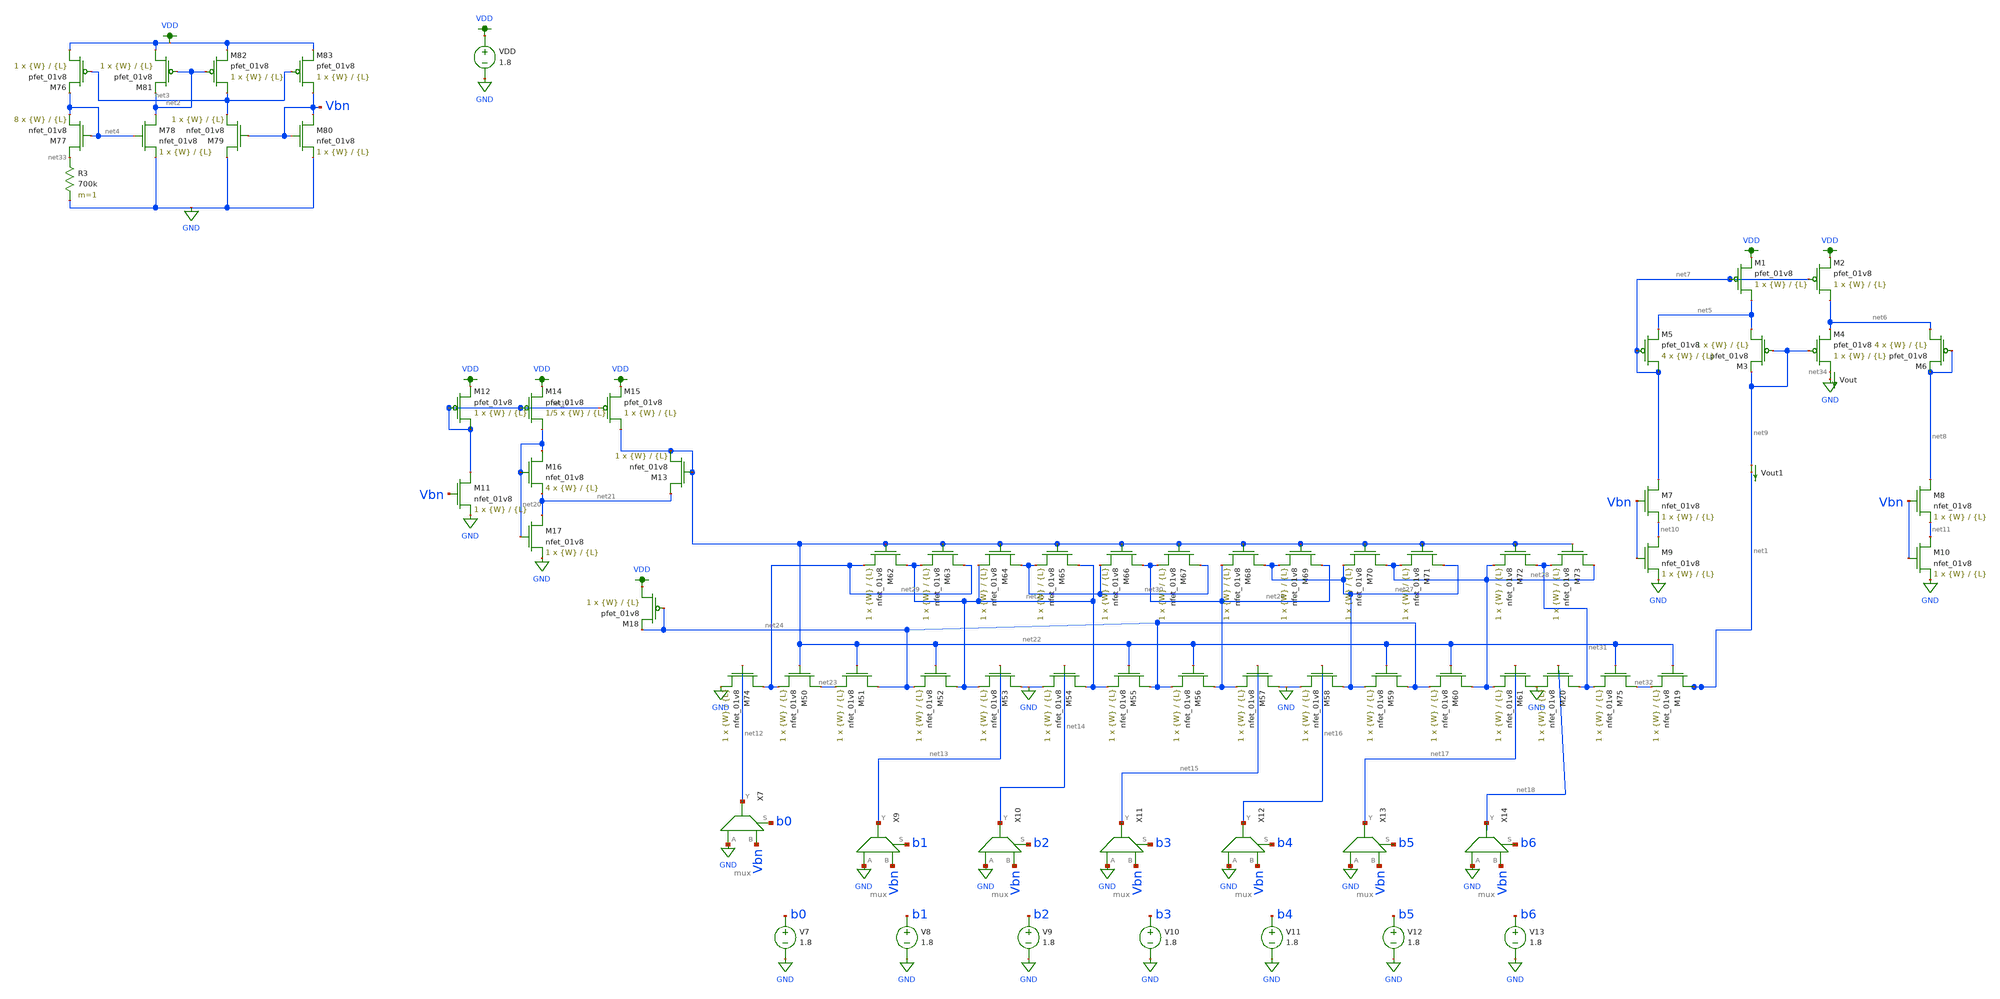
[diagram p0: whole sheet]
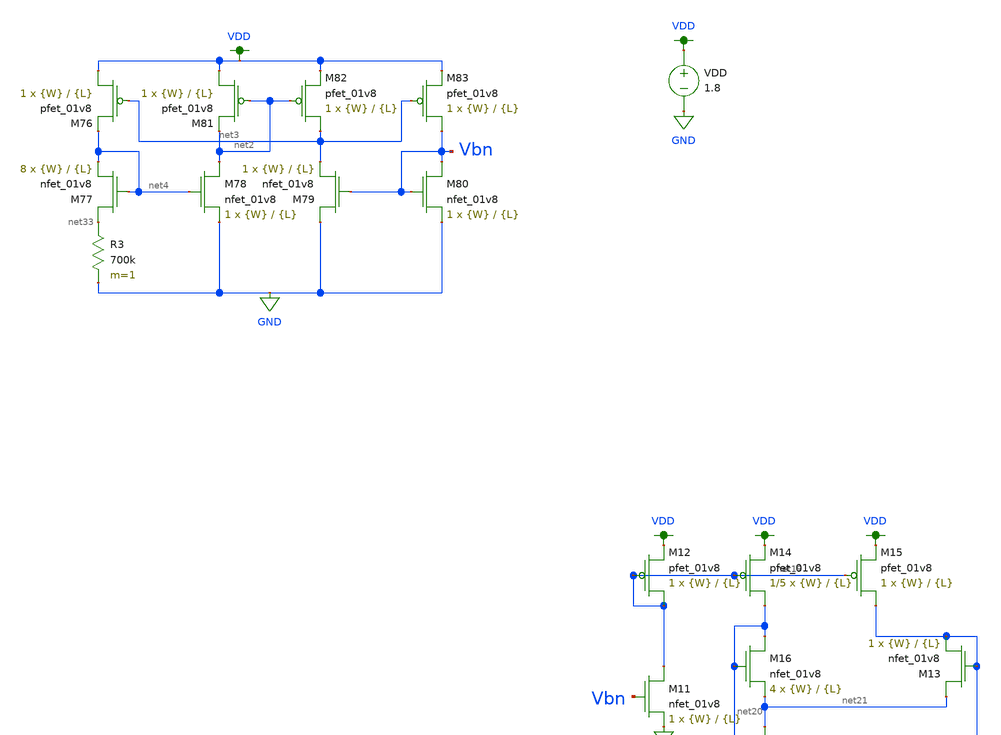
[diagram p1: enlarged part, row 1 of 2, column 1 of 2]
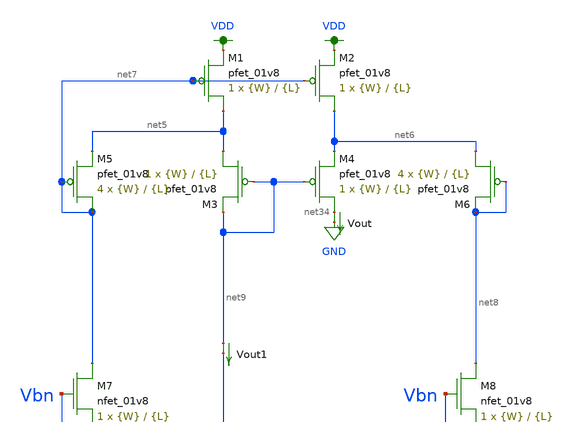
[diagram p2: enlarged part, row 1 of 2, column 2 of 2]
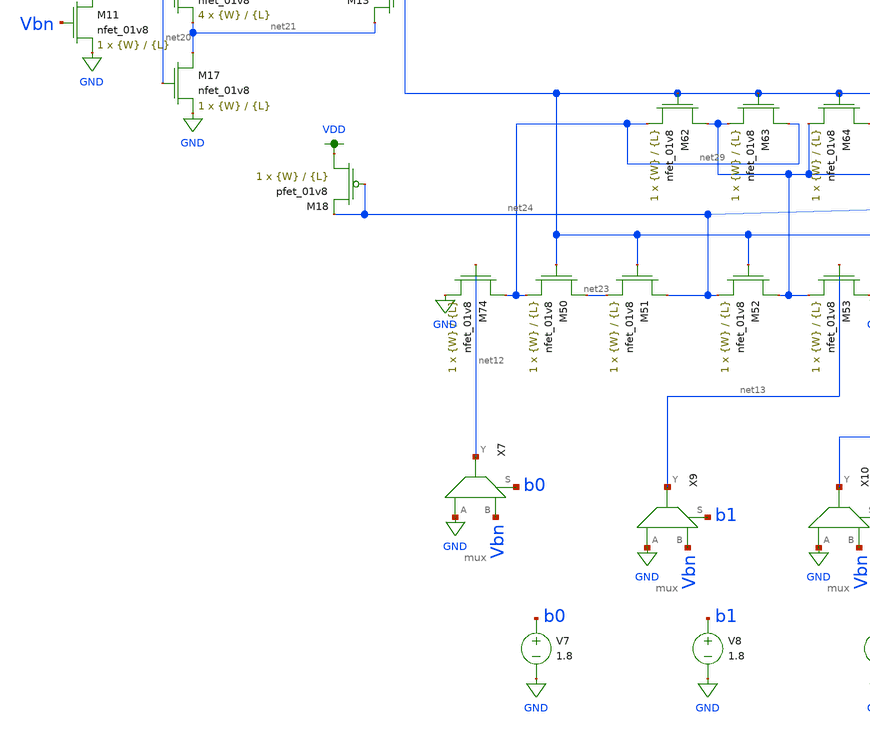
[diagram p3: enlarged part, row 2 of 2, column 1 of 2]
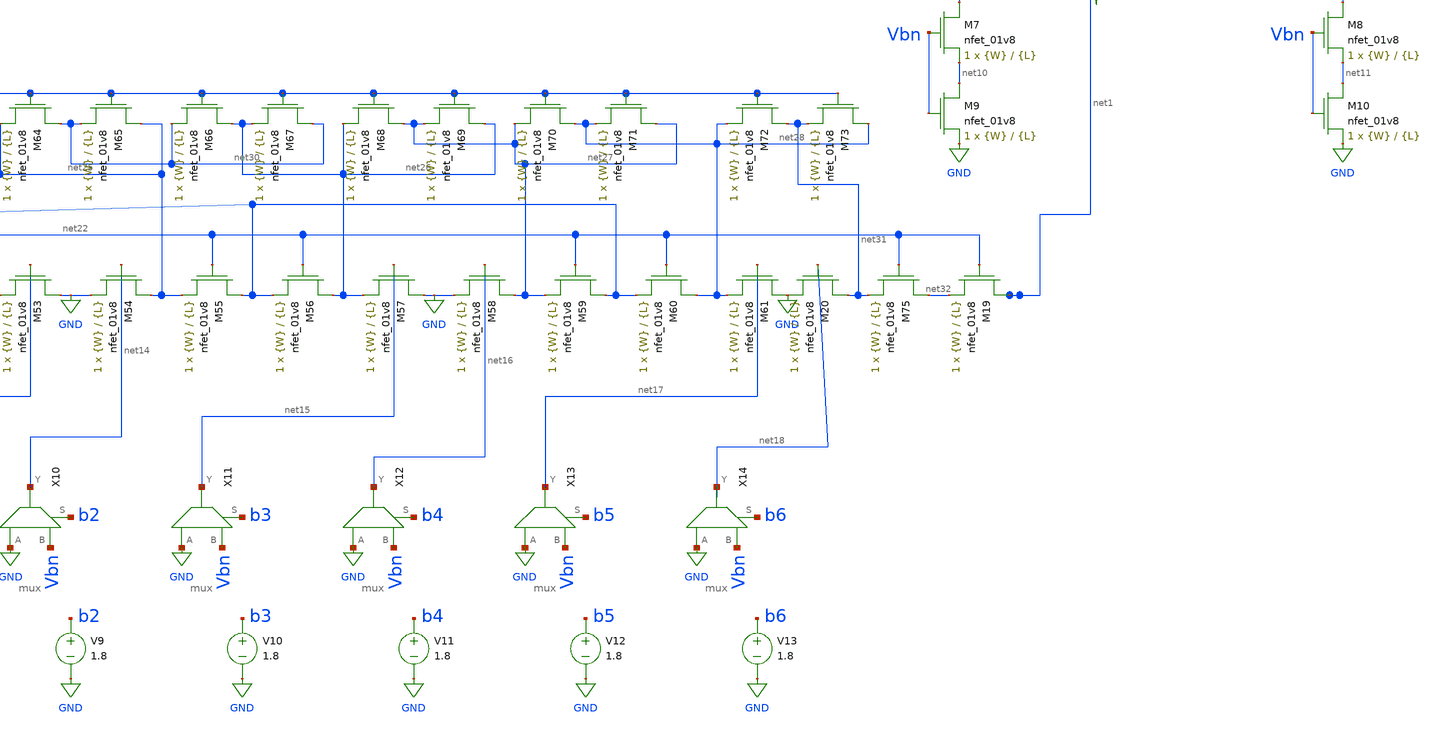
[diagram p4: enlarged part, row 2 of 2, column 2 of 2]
** sch_path: dac/schematics/misc/dac_lds_sim.sch
**.subckt dac_lds_sim
VDD VDD GND 1.8
XM76 VDD net3 net4 VDD sky130_fd_pr__pfet_01v8 L={L} W={W} nf=1 ad='int((nf+1)/2) * W/nf * 0.29' as='int((nf+2)/2) * W/nf * 0.29'
+ pd='2*int((nf+1)/2) * (W/nf + 0.29)' ps='2*int((nf+2)/2) * (W/nf + 0.29)' nrd='0.29 / W' nrs='0.29 / W'
+ sa=0 sb=0 sd=0 mult=1 m=1
XM77 net33 net4 net4 GND sky130_fd_pr__nfet_01v8 L={L} W={W} nf=1 ad='int((nf+1)/2) * W/nf * 0.29' as='int((nf+2)/2) * W/nf * 0.29'
+ pd='2*int((nf+1)/2) * (W/nf + 0.29)' ps='2*int((nf+2)/2) * (W/nf + 0.29)' nrd='0.29 / W' nrs='0.29 / W'
+ sa=0 sb=0 sd=0 mult=8 m=8
R3 net33 GND 700k m=1
XM78 net2 net4 GND GND sky130_fd_pr__nfet_01v8 L={L} W={W} nf=1 ad='int((nf+1)/2) * W/nf * 0.29' as='int((nf+2)/2) * W/nf * 0.29'
+ pd='2*int((nf+1)/2) * (W/nf + 0.29)' ps='2*int((nf+2)/2) * (W/nf + 0.29)' nrd='0.29 / W' nrs='0.29 / W'
+ sa=0 sb=0 sd=0 mult=1 m=1
XM79 GND Vbn net3 GND sky130_fd_pr__nfet_01v8 L={L} W={W} nf=1 ad='int((nf+1)/2) * W/nf * 0.29' as='int((nf+2)/2) * W/nf * 0.29'
+ pd='2*int((nf+1)/2) * (W/nf + 0.29)' ps='2*int((nf+2)/2) * (W/nf + 0.29)' nrd='0.29 / W' nrs='0.29 / W'
+ sa=0 sb=0 sd=0 mult=1 m=1
XM80 Vbn Vbn GND GND sky130_fd_pr__nfet_01v8 L={L} W={W} nf=1 ad='int((nf+1)/2) * W/nf * 0.29' as='int((nf+2)/2) * W/nf * 0.29'
+ pd='2*int((nf+1)/2) * (W/nf + 0.29)' ps='2*int((nf+2)/2) * (W/nf + 0.29)' nrd='0.29 / W' nrs='0.29 / W'
+ sa=0 sb=0 sd=0 mult=1 m=1
XM81 VDD net2 net2 VDD sky130_fd_pr__pfet_01v8 L={L} W={W} nf=1 ad='int((nf+1)/2) * W/nf * 0.29' as='int((nf+2)/2) * W/nf * 0.29'
+ pd='2*int((nf+1)/2) * (W/nf + 0.29)' ps='2*int((nf+2)/2) * (W/nf + 0.29)' nrd='0.29 / W' nrs='0.29 / W'
+ sa=0 sb=0 sd=0 mult=1 m=1
XM82 net3 net2 VDD VDD sky130_fd_pr__pfet_01v8 L={L} W={W} nf=1 ad='int((nf+1)/2) * W/nf * 0.29' as='int((nf+2)/2) * W/nf * 0.29'
+ pd='2*int((nf+1)/2) * (W/nf + 0.29)' ps='2*int((nf+2)/2) * (W/nf + 0.29)' nrd='0.29 / W' nrs='0.29 / W'
+ sa=0 sb=0 sd=0 mult=1 m=1
XM83 Vbn net3 VDD VDD sky130_fd_pr__pfet_01v8 L={L} W={W} nf=1 ad='int((nf+1)/2) * W/nf * 0.29' as='int((nf+2)/2) * W/nf * 0.29'
+ pd='2*int((nf+1)/2) * (W/nf + 0.29)' ps='2*int((nf+2)/2) * (W/nf + 0.29)' nrd='0.29 / W' nrs='0.29 / W'
+ sa=0 sb=0 sd=0 mult=1 m=1
Vout net34 GND 0
.save i(vout)
XM1 net5 net7 VDD VDD sky130_fd_pr__pfet_01v8 L={L} W={W} nf=1 ad='int((nf+1)/2) * W/nf * 0.29' as='int((nf+2)/2) * W/nf * 0.29'
+ pd='2*int((nf+1)/2) * (W/nf + 0.29)' ps='2*int((nf+2)/2) * (W/nf + 0.29)' nrd='0.29 / W' nrs='0.29 / W'
+ sa=0 sb=0 sd=0 mult=1 m=1
XM2 net6 net7 VDD VDD sky130_fd_pr__pfet_01v8 L={L} W={W} nf=1 ad='int((nf+1)/2) * W/nf * 0.29' as='int((nf+2)/2) * W/nf * 0.29'
+ pd='2*int((nf+1)/2) * (W/nf + 0.29)' ps='2*int((nf+2)/2) * (W/nf + 0.29)' nrd='0.29 / W' nrs='0.29 / W'
+ sa=0 sb=0 sd=0 mult=1 m=1
XM3 net5 net9 net9 VDD sky130_fd_pr__pfet_01v8 L={L} W={W} nf=1 ad='int((nf+1)/2) * W/nf * 0.29' as='int((nf+2)/2) * W/nf * 0.29'
+ pd='2*int((nf+1)/2) * (W/nf + 0.29)' ps='2*int((nf+2)/2) * (W/nf + 0.29)' nrd='0.29 / W' nrs='0.29 / W'
+ sa=0 sb=0 sd=0 mult=1 m=1
XM4 net34 net9 net6 VDD sky130_fd_pr__pfet_01v8 L={L} W={W} nf=1 ad='int((nf+1)/2) * W/nf * 0.29' as='int((nf+2)/2) * W/nf * 0.29'
+ pd='2*int((nf+1)/2) * (W/nf + 0.29)' ps='2*int((nf+2)/2) * (W/nf + 0.29)' nrd='0.29 / W' nrs='0.29 / W'
+ sa=0 sb=0 sd=0 mult=1 m=1
XM5 net7 net7 net5 VDD sky130_fd_pr__pfet_01v8 L={L} W={W} nf=1 ad='int((nf+1)/2) * W/nf * 0.29' as='int((nf+2)/2) * W/nf * 0.29'
+ pd='2*int((nf+1)/2) * (W/nf + 0.29)' ps='2*int((nf+2)/2) * (W/nf + 0.29)' nrd='0.29 / W' nrs='0.29 / W'
+ sa=0 sb=0 sd=0 mult=4 m=4
XM6 net6 net8 net8 VDD sky130_fd_pr__pfet_01v8 L={L} W={W} nf=1 ad='int((nf+1)/2) * W/nf * 0.29' as='int((nf+2)/2) * W/nf * 0.29'
+ pd='2*int((nf+1)/2) * (W/nf + 0.29)' ps='2*int((nf+2)/2) * (W/nf + 0.29)' nrd='0.29 / W' nrs='0.29 / W'
+ sa=0 sb=0 sd=0 mult=4 m=4
XM7 net7 Vbn net10 GND sky130_fd_pr__nfet_01v8 L={L} W={W} nf=1 ad='int((nf+1)/2) * W/nf * 0.29' as='int((nf+2)/2) * W/nf * 0.29'
+ pd='2*int((nf+1)/2) * (W/nf + 0.29)' ps='2*int((nf+2)/2) * (W/nf + 0.29)' nrd='0.29 / W' nrs='0.29 / W'
+ sa=0 sb=0 sd=0 mult=1 m=1
XM8 net8 Vbn net11 GND sky130_fd_pr__nfet_01v8 L={L} W={W} nf=1 ad='int((nf+1)/2) * W/nf * 0.29' as='int((nf+2)/2) * W/nf * 0.29'
+ pd='2*int((nf+1)/2) * (W/nf + 0.29)' ps='2*int((nf+2)/2) * (W/nf + 0.29)' nrd='0.29 / W' nrs='0.29 / W'
+ sa=0 sb=0 sd=0 mult=1 m=1
XM9 net10 Vbn GND GND sky130_fd_pr__nfet_01v8 L={L} W={W} nf=1 ad='int((nf+1)/2) * W/nf * 0.29' as='int((nf+2)/2) * W/nf * 0.29'
+ pd='2*int((nf+1)/2) * (W/nf + 0.29)' ps='2*int((nf+2)/2) * (W/nf + 0.29)' nrd='0.29 / W' nrs='0.29 / W'
+ sa=0 sb=0 sd=0 mult=1 m=1
XM10 net11 Vbn GND GND sky130_fd_pr__nfet_01v8 L={L} W={W} nf=1 ad='int((nf+1)/2) * W/nf * 0.29' as='int((nf+2)/2) * W/nf * 0.29'
+ pd='2*int((nf+1)/2) * (W/nf + 0.29)' ps='2*int((nf+2)/2) * (W/nf + 0.29)' nrd='0.29 / W' nrs='0.29 / W'
+ sa=0 sb=0 sd=0 mult=1 m=1
V7 b0 GND 1.8
V8 b1 GND 1.8
V9 b2 GND 1.8
V10 b3 GND 1.8
V11 b4 GND 1.8
V12 b5 GND 1.8
V13 b6 GND 1.8
X7 GND Vbn net12 b0 mux
X9 GND Vbn net13 b1 mux
X10 GND Vbn net14 b2 mux
X11 GND Vbn net15 b3 mux
X12 GND Vbn net16 b4 mux
X13 GND Vbn net17 b5 mux
X14 GND Vbn net18 b6 mux
XM11 net19 Vbn GND GND sky130_fd_pr__nfet_01v8 L={L} W={W} nf=1 ad='int((nf+1)/2) * W/nf * 0.29' as='int((nf+2)/2) * W/nf * 0.29'
+ pd='2*int((nf+1)/2) * (W/nf + 0.29)' ps='2*int((nf+2)/2) * (W/nf + 0.29)' nrd='0.29 / W' nrs='0.29 / W'
+ sa=0 sb=0 sd=0 mult=1 m=1
XM12 net19 net19 VDD VDD sky130_fd_pr__pfet_01v8 L={L} W={W} nf=1 ad='int((nf+1)/2) * W/nf * 0.29' as='int((nf+2)/2) * W/nf * 0.29'
+ pd='2*int((nf+1)/2) * (W/nf + 0.29)' ps='2*int((nf+2)/2) * (W/nf + 0.29)' nrd='0.29 / W' nrs='0.29 / W'
+ sa=0 sb=0 sd=0 mult=1 m=1
XM13 net21 net22 net22 GND sky130_fd_pr__nfet_01v8 L={L} W={W} nf=1 ad='int((nf+1)/2) * W/nf * 0.29'
+ as='int((nf+2)/2) * W/nf * 0.29' pd='2*int((nf+1)/2) * (W/nf + 0.29)' ps='2*int((nf+2)/2) * (W/nf + 0.29)'
+ nrd='0.29 / W' nrs='0.29 / W' sa=0 sb=0 sd=0 mult=1 m=1
XM14 net20 net19 VDD VDD sky130_fd_pr__pfet_01v8 L={L} W={W} nf=1 ad='int((nf+1)/2) * W/nf * 0.29' as='int((nf+2)/2) * W/nf * 0.29'
+ pd='2*int((nf+1)/2) * (W/nf + 0.29)' ps='2*int((nf+2)/2) * (W/nf + 0.29)' nrd='0.29 / W' nrs='0.29 / W'
+ sa=0 sb=0 sd=0 mult=1/5 m=1/5
XM15 net22 net19 VDD VDD sky130_fd_pr__pfet_01v8 L={L} W={W} nf=1 ad='int((nf+1)/2) * W/nf * 0.29' as='int((nf+2)/2) * W/nf * 0.29'
+ pd='2*int((nf+1)/2) * (W/nf + 0.29)' ps='2*int((nf+2)/2) * (W/nf + 0.29)' nrd='0.29 / W' nrs='0.29 / W'
+ sa=0 sb=0 sd=0 mult=1 m=1
XM16 net20 net20 net21 GND sky130_fd_pr__nfet_01v8 L={L} W={W} nf=1 ad='int((nf+1)/2) * W/nf * 0.29'
+ as='int((nf+2)/2) * W/nf * 0.29' pd='2*int((nf+1)/2) * (W/nf + 0.29)' ps='2*int((nf+2)/2) * (W/nf + 0.29)'
+ nrd='0.29 / W' nrs='0.29 / W' sa=0 sb=0 sd=0 mult=4 m=4
XM17 net21 net20 GND GND sky130_fd_pr__nfet_01v8 L={L} W={W} nf=1 ad='int((nf+1)/2) * W/nf * 0.29' as='int((nf+2)/2) * W/nf * 0.29'
+ pd='2*int((nf+1)/2) * (W/nf + 0.29)' ps='2*int((nf+2)/2) * (W/nf + 0.29)' nrd='0.29 / W' nrs='0.29 / W'
+ sa=0 sb=0 sd=0 mult=1 m=1
Vout1 net9 net1 0
.save i(vout1)
XM50 net23 net22 net29 GND sky130_fd_pr__nfet_01v8 L={L} W={W} nf=1 ad='int((nf+1)/2) * W/nf * 0.29'
+ as='int((nf+2)/2) * W/nf * 0.29' pd='2*int((nf+1)/2) * (W/nf + 0.29)' ps='2*int((nf+2)/2) * (W/nf + 0.29)'
+ nrd='0.29 / W' nrs='0.29 / W' sa=0 sb=0 sd=0 mult=1 m=1
XM51 net24 net22 net23 GND sky130_fd_pr__nfet_01v8 L={L} W={W} nf=1 ad='int((nf+1)/2) * W/nf * 0.29'
+ as='int((nf+2)/2) * W/nf * 0.29' pd='2*int((nf+1)/2) * (W/nf + 0.29)' ps='2*int((nf+2)/2) * (W/nf + 0.29)'
+ nrd='0.29 / W' nrs='0.29 / W' sa=0 sb=0 sd=0 mult=1 m=1
XM52 net25 net22 net24 GND sky130_fd_pr__nfet_01v8 L={L} W={W} nf=1 ad='int((nf+1)/2) * W/nf * 0.29'
+ as='int((nf+2)/2) * W/nf * 0.29' pd='2*int((nf+1)/2) * (W/nf + 0.29)' ps='2*int((nf+2)/2) * (W/nf + 0.29)'
+ nrd='0.29 / W' nrs='0.29 / W' sa=0 sb=0 sd=0 mult=1 m=1
XM53 GND net13 net25 GND sky130_fd_pr__nfet_01v8 L={L} W={W} nf=1 ad='int((nf+1)/2) * W/nf * 0.29' as='int((nf+2)/2) * W/nf * 0.29'
+ pd='2*int((nf+1)/2) * (W/nf + 0.29)' ps='2*int((nf+2)/2) * (W/nf + 0.29)' nrd='0.29 / W' nrs='0.29 / W'
+ sa=0 sb=0 sd=0 mult=1 m=1
XM54 net25 net14 GND GND sky130_fd_pr__nfet_01v8 L={L} W={W} nf=1 ad='int((nf+1)/2) * W/nf * 0.29' as='int((nf+2)/2) * W/nf * 0.29'
+ pd='2*int((nf+1)/2) * (W/nf + 0.29)' ps='2*int((nf+2)/2) * (W/nf + 0.29)' nrd='0.29 / W' nrs='0.29 / W'
+ sa=0 sb=0 sd=0 mult=1 m=1
XM55 net24 net22 net25 GND sky130_fd_pr__nfet_01v8 L={L} W={W} nf=1 ad='int((nf+1)/2) * W/nf * 0.29'
+ as='int((nf+2)/2) * W/nf * 0.29' pd='2*int((nf+1)/2) * (W/nf + 0.29)' ps='2*int((nf+2)/2) * (W/nf + 0.29)'
+ nrd='0.29 / W' nrs='0.29 / W' sa=0 sb=0 sd=0 mult=1 m=1
XM56 net26 net22 net24 GND sky130_fd_pr__nfet_01v8 L={L} W={W} nf=1 ad='int((nf+1)/2) * W/nf * 0.29'
+ as='int((nf+2)/2) * W/nf * 0.29' pd='2*int((nf+1)/2) * (W/nf + 0.29)' ps='2*int((nf+2)/2) * (W/nf + 0.29)'
+ nrd='0.29 / W' nrs='0.29 / W' sa=0 sb=0 sd=0 mult=1 m=1
XM57 GND net15 net26 GND sky130_fd_pr__nfet_01v8 L={L} W={W} nf=1 ad='int((nf+1)/2) * W/nf * 0.29' as='int((nf+2)/2) * W/nf * 0.29'
+ pd='2*int((nf+1)/2) * (W/nf + 0.29)' ps='2*int((nf+2)/2) * (W/nf + 0.29)' nrd='0.29 / W' nrs='0.29 / W'
+ sa=0 sb=0 sd=0 mult=1 m=1
XM58 net27 net16 GND GND sky130_fd_pr__nfet_01v8 L={L} W={W} nf=1 ad='int((nf+1)/2) * W/nf * 0.29' as='int((nf+2)/2) * W/nf * 0.29'
+ pd='2*int((nf+1)/2) * (W/nf + 0.29)' ps='2*int((nf+2)/2) * (W/nf + 0.29)' nrd='0.29 / W' nrs='0.29 / W'
+ sa=0 sb=0 sd=0 mult=1 m=1
XM59 net24 net22 net27 GND sky130_fd_pr__nfet_01v8 L={L} W={W} nf=1 ad='int((nf+1)/2) * W/nf * 0.29'
+ as='int((nf+2)/2) * W/nf * 0.29' pd='2*int((nf+1)/2) * (W/nf + 0.29)' ps='2*int((nf+2)/2) * (W/nf + 0.29)'
+ nrd='0.29 / W' nrs='0.29 / W' sa=0 sb=0 sd=0 mult=1 m=1
XM60 net28 net22 net24 GND sky130_fd_pr__nfet_01v8 L={L} W={W} nf=1 ad='int((nf+1)/2) * W/nf * 0.29'
+ as='int((nf+2)/2) * W/nf * 0.29' pd='2*int((nf+1)/2) * (W/nf + 0.29)' ps='2*int((nf+2)/2) * (W/nf + 0.29)'
+ nrd='0.29 / W' nrs='0.29 / W' sa=0 sb=0 sd=0 mult=1 m=1
XM61 GND net17 net28 GND sky130_fd_pr__nfet_01v8 L={L} W={W} nf=1 ad='int((nf+1)/2) * W/nf * 0.29' as='int((nf+2)/2) * W/nf * 0.29'
+ pd='2*int((nf+1)/2) * (W/nf + 0.29)' ps='2*int((nf+2)/2) * (W/nf + 0.29)' nrd='0.29 / W' nrs='0.29 / W'
+ sa=0 sb=0 sd=0 mult=1 m=1
XM62 net25 net22 net29 GND sky130_fd_pr__nfet_01v8 L={L} W={W} nf=1 ad='int((nf+1)/2) * W/nf * 0.29'
+ as='int((nf+2)/2) * W/nf * 0.29' pd='2*int((nf+1)/2) * (W/nf + 0.29)' ps='2*int((nf+2)/2) * (W/nf + 0.29)'
+ nrd='0.29 / W' nrs='0.29 / W' sa=0 sb=0 sd=0 mult=1 m=1
XM63 net29 net22 net25 GND sky130_fd_pr__nfet_01v8 L={L} W={W} nf=1 ad='int((nf+1)/2) * W/nf * 0.29'
+ as='int((nf+2)/2) * W/nf * 0.29' pd='2*int((nf+1)/2) * (W/nf + 0.29)' ps='2*int((nf+2)/2) * (W/nf + 0.29)'
+ nrd='0.29 / W' nrs='0.29 / W' sa=0 sb=0 sd=0 mult=1 m=1
XM64 net30 net22 net25 GND sky130_fd_pr__nfet_01v8 L={L} W={W} nf=1 ad='int((nf+1)/2) * W/nf * 0.29'
+ as='int((nf+2)/2) * W/nf * 0.29' pd='2*int((nf+1)/2) * (W/nf + 0.29)' ps='2*int((nf+2)/2) * (W/nf + 0.29)'
+ nrd='0.29 / W' nrs='0.29 / W' sa=0 sb=0 sd=0 mult=1 m=1
XM65 net25 net22 net30 GND sky130_fd_pr__nfet_01v8 L={L} W={W} nf=1 ad='int((nf+1)/2) * W/nf * 0.29'
+ as='int((nf+2)/2) * W/nf * 0.29' pd='2*int((nf+1)/2) * (W/nf + 0.29)' ps='2*int((nf+2)/2) * (W/nf + 0.29)'
+ nrd='0.29 / W' nrs='0.29 / W' sa=0 sb=0 sd=0 mult=1 m=1
XM66 net26 net22 net30 GND sky130_fd_pr__nfet_01v8 L={L} W={W} nf=1 ad='int((nf+1)/2) * W/nf * 0.29'
+ as='int((nf+2)/2) * W/nf * 0.29' pd='2*int((nf+1)/2) * (W/nf + 0.29)' ps='2*int((nf+2)/2) * (W/nf + 0.29)'
+ nrd='0.29 / W' nrs='0.29 / W' sa=0 sb=0 sd=0 mult=1 m=1
XM67 net30 net22 net26 GND sky130_fd_pr__nfet_01v8 L={L} W={W} nf=1 ad='int((nf+1)/2) * W/nf * 0.29'
+ as='int((nf+2)/2) * W/nf * 0.29' pd='2*int((nf+1)/2) * (W/nf + 0.29)' ps='2*int((nf+2)/2) * (W/nf + 0.29)'
+ nrd='0.29 / W' nrs='0.29 / W' sa=0 sb=0 sd=0 mult=1 m=1
XM68 net27 net22 net26 GND sky130_fd_pr__nfet_01v8 L={L} W={W} nf=1 ad='int((nf+1)/2) * W/nf * 0.29'
+ as='int((nf+2)/2) * W/nf * 0.29' pd='2*int((nf+1)/2) * (W/nf + 0.29)' ps='2*int((nf+2)/2) * (W/nf + 0.29)'
+ nrd='0.29 / W' nrs='0.29 / W' sa=0 sb=0 sd=0 mult=1 m=1
XM69 net26 net22 net27 GND sky130_fd_pr__nfet_01v8 L={L} W={W} nf=1 ad='int((nf+1)/2) * W/nf * 0.29'
+ as='int((nf+2)/2) * W/nf * 0.29' pd='2*int((nf+1)/2) * (W/nf + 0.29)' ps='2*int((nf+2)/2) * (W/nf + 0.29)'
+ nrd='0.29 / W' nrs='0.29 / W' sa=0 sb=0 sd=0 mult=1 m=1
XM70 net28 net22 net27 GND sky130_fd_pr__nfet_01v8 L={L} W={W} nf=1 ad='int((nf+1)/2) * W/nf * 0.29'
+ as='int((nf+2)/2) * W/nf * 0.29' pd='2*int((nf+1)/2) * (W/nf + 0.29)' ps='2*int((nf+2)/2) * (W/nf + 0.29)'
+ nrd='0.29 / W' nrs='0.29 / W' sa=0 sb=0 sd=0 mult=1 m=1
XM71 net27 net22 net28 GND sky130_fd_pr__nfet_01v8 L={L} W={W} nf=1 ad='int((nf+1)/2) * W/nf * 0.29'
+ as='int((nf+2)/2) * W/nf * 0.29' pd='2*int((nf+1)/2) * (W/nf + 0.29)' ps='2*int((nf+2)/2) * (W/nf + 0.29)'
+ nrd='0.29 / W' nrs='0.29 / W' sa=0 sb=0 sd=0 mult=1 m=1
XM72 net31 net22 net28 GND sky130_fd_pr__nfet_01v8 L={L} W={W} nf=1 ad='int((nf+1)/2) * W/nf * 0.29'
+ as='int((nf+2)/2) * W/nf * 0.29' pd='2*int((nf+1)/2) * (W/nf + 0.29)' ps='2*int((nf+2)/2) * (W/nf + 0.29)'
+ nrd='0.29 / W' nrs='0.29 / W' sa=0 sb=0 sd=0 mult=1 m=1
XM73 net28 net22 net31 GND sky130_fd_pr__nfet_01v8 L={L} W={W} nf=1 ad='int((nf+1)/2) * W/nf * 0.29'
+ as='int((nf+2)/2) * W/nf * 0.29' pd='2*int((nf+1)/2) * (W/nf + 0.29)' ps='2*int((nf+2)/2) * (W/nf + 0.29)'
+ nrd='0.29 / W' nrs='0.29 / W' sa=0 sb=0 sd=0 mult=1 m=1
XM74 net29 net12 GND GND sky130_fd_pr__nfet_01v8 L={L} W={W} nf=1 ad='int((nf+1)/2) * W/nf * 0.29' as='int((nf+2)/2) * W/nf * 0.29'
+ pd='2*int((nf+1)/2) * (W/nf + 0.29)' ps='2*int((nf+2)/2) * (W/nf + 0.29)' nrd='0.29 / W' nrs='0.29 / W'
+ sa=0 sb=0 sd=0 mult=1 m=1
XM75 net32 net22 net31 GND sky130_fd_pr__nfet_01v8 L={L} W={W} nf=1 ad='int((nf+1)/2) * W/nf * 0.29'
+ as='int((nf+2)/2) * W/nf * 0.29' pd='2*int((nf+1)/2) * (W/nf + 0.29)' ps='2*int((nf+2)/2) * (W/nf + 0.29)'
+ nrd='0.29 / W' nrs='0.29 / W' sa=0 sb=0 sd=0 mult=1 m=1
XM19 net1 net22 net32 GND sky130_fd_pr__nfet_01v8 L={L} W={W} nf=1 ad='int((nf+1)/2) * W/nf * 0.29' as='int((nf+2)/2) * W/nf * 0.29'
+ pd='2*int((nf+1)/2) * (W/nf + 0.29)' ps='2*int((nf+2)/2) * (W/nf + 0.29)' nrd='0.29 / W' nrs='0.29 / W'
+ sa=0 sb=0 sd=0 mult=1 m=1
XM20 net31 net18 GND GND sky130_fd_pr__nfet_01v8 L={L} W={W} nf=1 ad='int((nf+1)/2) * W/nf * 0.29' as='int((nf+2)/2) * W/nf * 0.29'
+ pd='2*int((nf+1)/2) * (W/nf + 0.29)' ps='2*int((nf+2)/2) * (W/nf + 0.29)' nrd='0.29 / W' nrs='0.29 / W'
+ sa=0 sb=0 sd=0 mult=1 m=1
XM18 VDD net24 net24 VDD sky130_fd_pr__pfet_01v8 L={L} W={W} nf=1 ad='int((nf+1)/2) * W/nf * 0.29' as='int((nf+2)/2) * W/nf * 0.29'
+ pd='2*int((nf+1)/2) * (W/nf + 0.29)' ps='2*int((nf+2)/2) * (W/nf + 0.29)' nrd='0.29 / W' nrs='0.29 / W'
+ sa=0 sb=0 sd=0 mult=1 m=1
**** begin user architecture code

.param W=32
.param L=4
.control
set wr_vecnames
set wr_singlescale
let code = 0
  while code < 128
    if code eq 0
      let b0 = 0
    else
      let b0 = code % 2 * 1.8
    end
    if floor(code / 2) eq 0
      let b1 = 0
    else
      let b1 = floor(code / 2) % 2 * 1.8
    end
    if floor(code / 4) eq 0
      let b2 = 0
    else
      let b2 = floor(code / 4) % 2 * 1.8
    end
    if floor(code / 8) eq 0
      let b3 = 0
    else
      let b3 = floor(code / 8) % 2 * 1.8
    end
    if floor(code / 16) eq 0
      let b4 = 0
    else
      let b4 = floor(code / 16) % 2 * 1.8
    end
    if floor(code / 32) eq 0
      let b5 = 0
    else
      let b5 = floor(code / 32) % 2 * 1.8
    end
    if floor(code / 64) eq 0
      let b6 = 0
    else
      let b6 = floor(code / 64) % 2 * 1.8
    end
    alter v7 $&b0
    alter v8 $&b1
    alter v9 $&b2
    alter v10 $&b3
    alter v11 $&b4
    alter v12 $&b5
    alter v13 $&b6
    save all
    op
    wrdata ~/Documents/current-output-dac-vlsi/simulations/dac_sim.txt v(Vbn) i(Vout) i(Vout1) v(b6)
+ v(b5) v(b4) v(b3) v(b2) v(b1) v(b0)
    if code eq 0
      set appendwrite
      set wr_vecnames = FALSE
    end
    let code = code + 1
  end
.endc


.option wnflag=1
.param MC_SWITCH=0.0
.lib ~/skywater/skywater-pdk/libraries/sky130_fd_pr_ngspice/latest/models/sky130.lib.spice tt

**** end user architecture code
**.ends

* expanding   symbol:  /home/madvlsi/Documents/current-output-dac-vlsi/schematics/mux.sym # of
*+ pins=4
** sym_path: dac/schematics/mux.sym
** sch_path: dac/schematics/mux.sch
.subckt mux A B Y S
*.ipin A
*.ipin B
*.ipin S
*.opin Y
XM1 A S Y VDD sky130_fd_pr__pfet_01v8 L=0.15 W=1 nf=1 ad='int((nf+1)/2) * W/nf * 0.29' as='int((nf+2)/2) * W/nf * 0.29'
+ pd='2*int((nf+1)/2) * (W/nf + 0.29)' ps='2*int((nf+2)/2) * (W/nf + 0.29)' nrd='0.29 / W' nrs='0.29 / W'
+ sa=0 sb=0 sd=0 mult=1 m=1
XM3 net1 S VDD VDD sky130_fd_pr__pfet_01v8 L=0.15 W=1 nf=1 ad='int((nf+1)/2) * W/nf * 0.29' as='int((nf+2)/2) * W/nf * 0.29'
+ pd='2*int((nf+1)/2) * (W/nf + 0.29)' ps='2*int((nf+2)/2) * (W/nf + 0.29)' nrd='0.29 / W' nrs='0.29 / W'
+ sa=0 sb=0 sd=0 mult=1 m=1
XM4 net1 S GND GND sky130_fd_pr__nfet_01v8 L=0.15 W=1 nf=1 ad='int((nf+1)/2) * W/nf * 0.29' as='int((nf+2)/2) * W/nf * 0.29'
+ pd='2*int((nf+1)/2) * (W/nf + 0.29)' ps='2*int((nf+2)/2) * (W/nf + 0.29)' nrd='0.29 / W' nrs='0.29 / W'
+ sa=0 sb=0 sd=0 mult=1 m=1
XM5 A net1 Y GND sky130_fd_pr__nfet_01v8 L=0.15 W=1 nf=1 ad='int((nf+1)/2) * W/nf * 0.29' as='int((nf+2)/2) * W/nf * 0.29'
+ pd='2*int((nf+1)/2) * (W/nf + 0.29)' ps='2*int((nf+2)/2) * (W/nf + 0.29)' nrd='0.29 / W' nrs='0.29 / W'
+ sa=0 sb=0 sd=0 mult=1 m=1
XM2 B net1 Y VDD sky130_fd_pr__pfet_01v8 L=0.15 W=1 nf=1 ad='int((nf+1)/2) * W/nf * 0.29' as='int((nf+2)/2) * W/nf * 0.29'
+ pd='2*int((nf+1)/2) * (W/nf + 0.29)' ps='2*int((nf+2)/2) * (W/nf + 0.29)' nrd='0.29 / W' nrs='0.29 / W'
+ sa=0 sb=0 sd=0 mult=1 m=1
XM6 B S Y GND sky130_fd_pr__nfet_01v8 L=0.15 W=1 nf=1 ad='int((nf+1)/2) * W/nf * 0.29' as='int((nf+2)/2) * W/nf * 0.29'
+ pd='2*int((nf+1)/2) * (W/nf + 0.29)' ps='2*int((nf+2)/2) * (W/nf + 0.29)' nrd='0.29 / W' nrs='0.29 / W'
+ sa=0 sb=0 sd=0 mult=1 m=1
.ends

.GLOBAL GND
.GLOBAL VDD
.end
